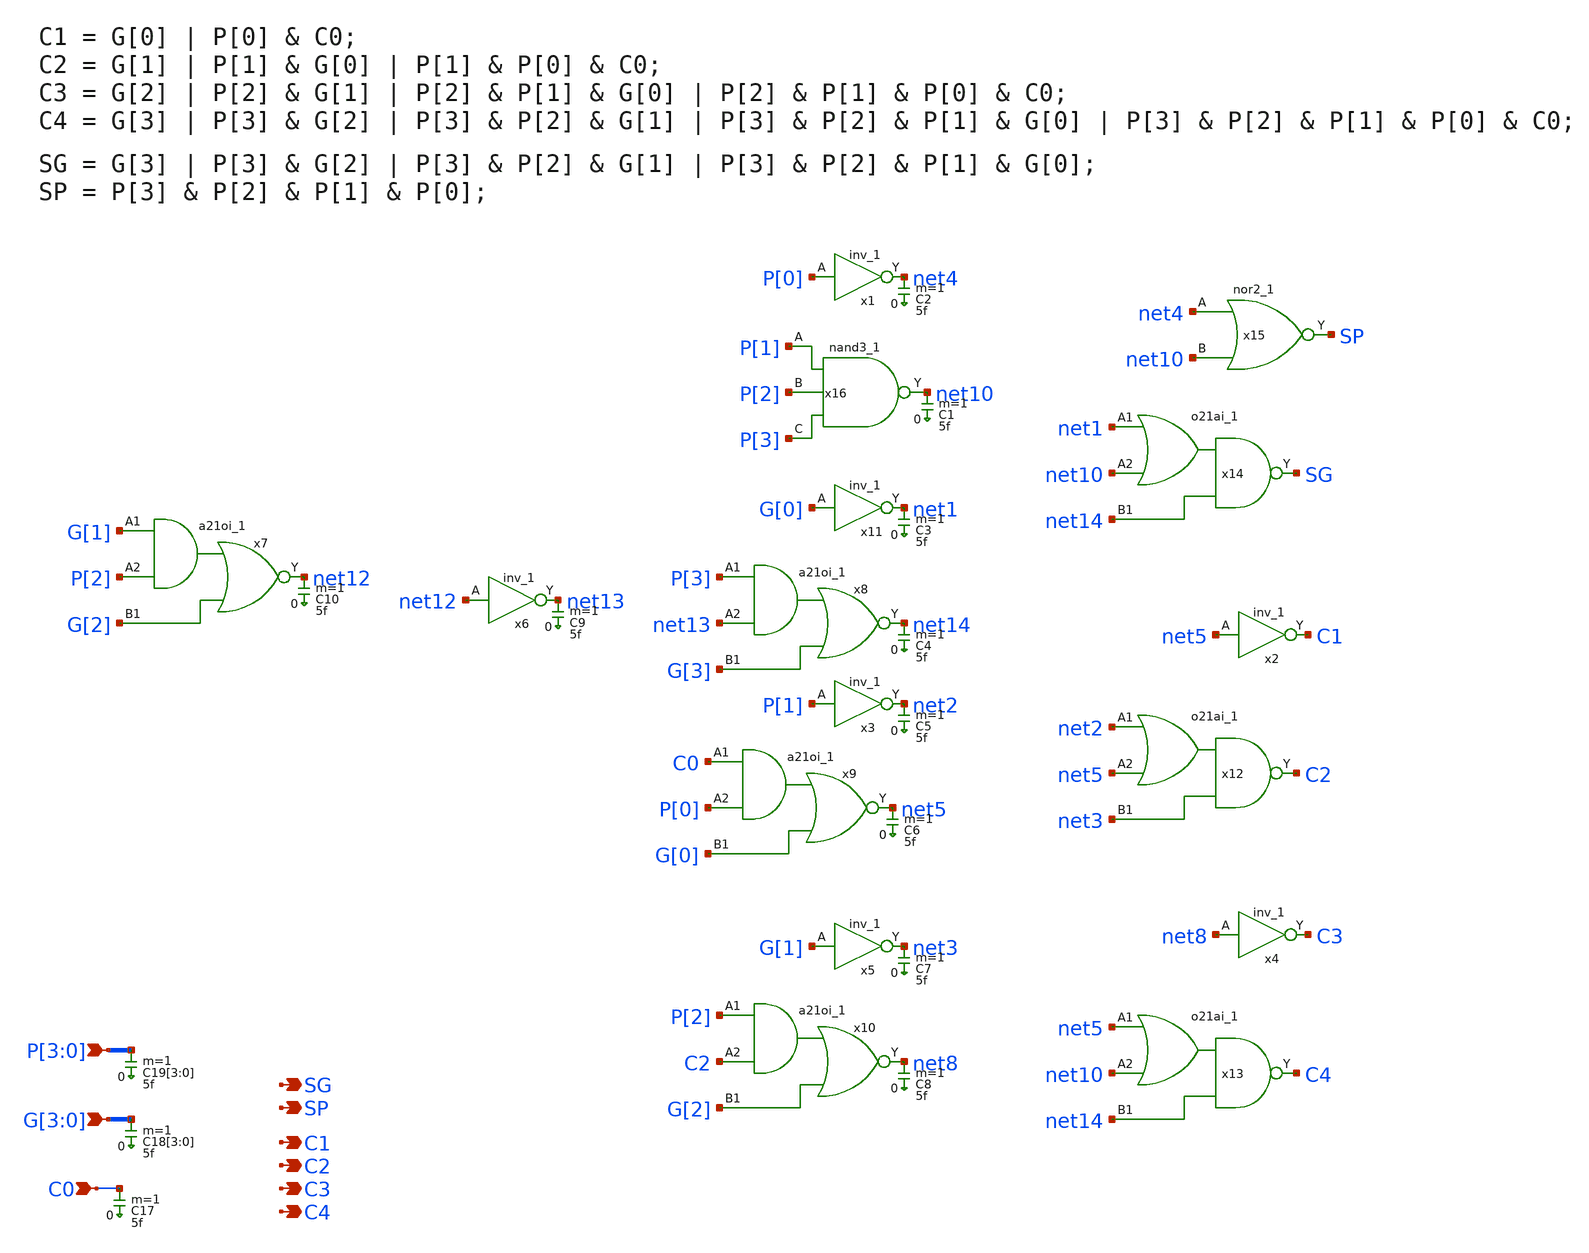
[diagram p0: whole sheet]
** sch_path: sky130A/xschem_libs/sky130_tests/cla_4bits/schematic/cla_4bits.sch
**.subckt cla_4bits P[3],P[2],P[1],P[0] G[3],G[2],G[1],G[0] C0 C4 C3 C2 C1 SG SP
*.ipin P[3],P[2],P[1],P[0]
*.ipin G[3],G[2],G[1],G[0]
*.ipin C0
*.opin C4
*.opin C3
*.opin C2
*.opin C1
*.opin SG
*.opin SP
x1 P[0] VSS VSS VCC VCC net4 sky130_fd_sc_hd__inv_1
x2 net5 VSS VSS VCC VCC C1 sky130_fd_sc_hd__inv_1
x3 P[1] VSS VSS VCC VCC net2 sky130_fd_sc_hd__inv_1
x4 net8 VSS VSS VCC VCC C3 sky130_fd_sc_hd__inv_1
x5 G[1] VSS VSS VCC VCC net3 sky130_fd_sc_hd__inv_1
x6 net12 VSS VSS VCC VCC net13 sky130_fd_sc_hd__inv_1
x7 G[1] P[2] G[2] VSS VSS VCC VCC net12 sky130_fd_sc_hd__a21oi_1
x8 P[3] net13 G[3] VSS VSS VCC VCC net14 sky130_fd_sc_hd__a21oi_1
x9 C0 P[0] G[0] VSS VSS VCC VCC net5 sky130_fd_sc_hd__a21oi_1
x10 P[2] C2 G[2] VSS VSS VCC VCC net8 sky130_fd_sc_hd__a21oi_1
x11 G[0] VSS VSS VCC VCC net1 sky130_fd_sc_hd__inv_1
x12 net2 net5 net3 VSS VSS VCC VCC C2 sky130_fd_sc_hd__o21ai_1
x13 net5 net10 net14 VSS VSS VCC VCC C4 sky130_fd_sc_hd__o21ai_1
x14 net1 net10 net14 VSS VSS VCC VCC SG sky130_fd_sc_hd__o21ai_1
x15 net4 net10 VSS VSS VCC VCC SP sky130_fd_sc_hd__nor2_1
x16 P[1] P[2] P[3] VSS VSS VCC VCC net10 sky130_fd_sc_hd__nand3_1
C2 net4 0 5f m=1
C1 net10 0 5f m=1
C3 net1 0 5f m=1
C4 net14 0 5f m=1
C5 net2 0 5f m=1
C6 net5 0 5f m=1
C7 net3 0 5f m=1
C8 net8 0 5f m=1
C9 net13 0 5f m=1
C10 net12 0 5f m=1
C19[3] P[3] 0 5f m=1
C19[2] P[2] 0 5f m=1
C19[1] P[1] 0 5f m=1
C19[0] P[0] 0 5f m=1
C18[3] G[3] 0 5f m=1
C18[2] G[2] 0 5f m=1
C18[1] G[1] 0 5f m=1
C18[0] G[0] 0 5f m=1
C17 C0 0 5f m=1
**.ends
.end
